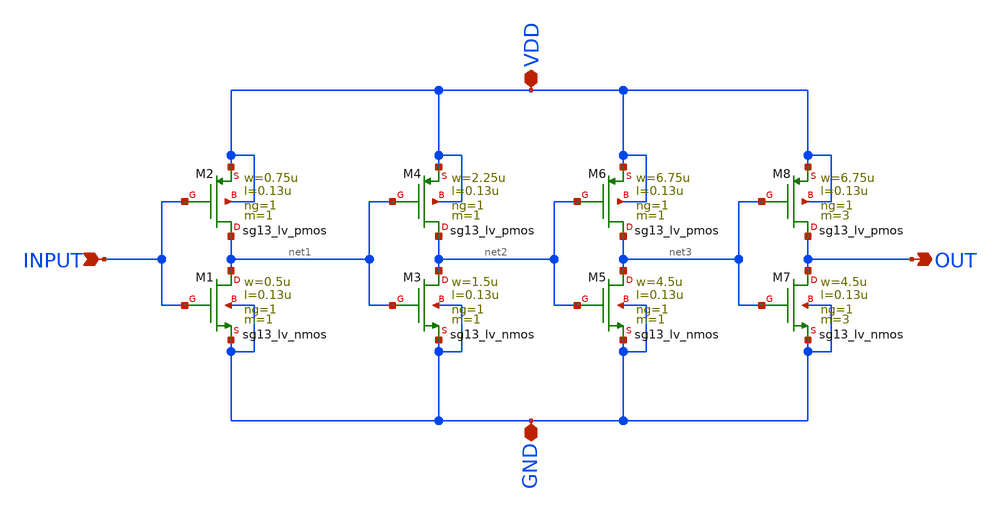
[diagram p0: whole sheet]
** sch_path: schematics/buf/buf.sch
**.subckt buf INPUT VDD GND OUT
*.ipin INPUT
*.iopin VDD
*.iopin GND
*.opin OUT
XM1 net1 INPUT GND GND sg13_lv_nmos w=0.5u l=0.13u ng=1 m=1 mm_ok=1
XM2 net1 INPUT VDD VDD sg13_lv_pmos w=0.75u l=0.13u ng=1 m=1 mm_ok=1
XM3 net2 net1 GND GND sg13_lv_nmos w=1.5u l=0.13u ng=1 m=1 mm_ok=1
XM4 net2 net1 VDD VDD sg13_lv_pmos w=2.25u l=0.13u ng=1 m=1 mm_ok=1
XM5 net3 net2 GND GND sg13_lv_nmos w=4.5u l=0.13u ng=1 m=1 mm_ok=1
XM6 net3 net2 VDD VDD sg13_lv_pmos w=6.75u l=0.13u ng=1 m=1 mm_ok=1
XM7 OUT net3 GND GND sg13_lv_nmos w=4.5u l=0.13u ng=1 m=3 mm_ok=1
XM8 OUT net3 VDD VDD sg13_lv_pmos w=6.75u l=0.13u ng=1 m=3 mm_ok=1
**.ends
.end
